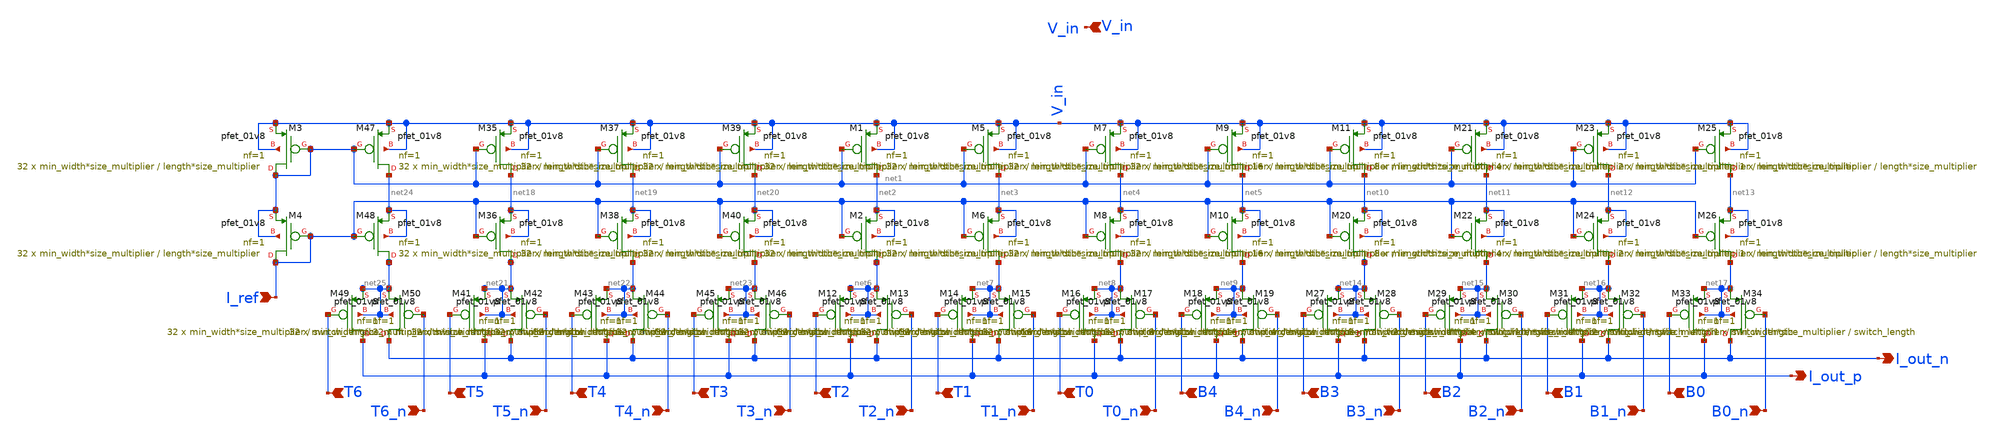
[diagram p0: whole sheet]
** sch_path: analog/schematics/components/DAC/segmented_dac.sch
**.subckt segmented_dac B0 B0_n B1 B2 B3 B1_n B2_n B3_n B4 B4_n T0 T1 T2 T0_n T1_n T2_n I_out_p V_in
*+ I_out_n T3 T4 T5 T3_n T4_n T5_n T6 T6_n I_ref
*.ipin B0
*.ipin B0_n
*.ipin B1
*.ipin B2
*.ipin B3
*.ipin B1_n
*.ipin B2_n
*.ipin B3_n
*.ipin B4
*.ipin B4_n
*.ipin T0
*.ipin T1
*.ipin T2
*.ipin T0_n
*.ipin T1_n
*.ipin T2_n
*.opin I_out_p
*.ipin V_in
*.opin I_out_n
*.ipin T3
*.ipin T4
*.ipin T5
*.ipin T3_n
*.ipin T4_n
*.ipin T5_n
*.ipin T6
*.ipin T6_n
*.ipin I_ref
XM1 net2 net1 V_in V_in sky130_fd_pr__pfet_01v8 L=length*size_multiplier W=min_width*size_multiplier
+ nf=1 ad='int((nf+1)/2) * W/nf * 0.29' as='int((nf+2)/2) * W/nf * 0.29' pd='2*int((nf+1)/2) * (W/nf + 0.29)'
+ ps='2*int((nf+2)/2) * (W/nf + 0.29)' nrd='0.29 / W' nrs='0.29 / W' sa=0 sb=0 sd=0 mult=32 m=32
XM2 net6 I_ref net2 net2 sky130_fd_pr__pfet_01v8 L=length*size_multiplier W=min_width*size_multiplier
+ nf=1 ad='int((nf+1)/2) * W/nf * 0.29' as='int((nf+2)/2) * W/nf * 0.29' pd='2*int((nf+1)/2) * (W/nf + 0.29)'
+ ps='2*int((nf+2)/2) * (W/nf + 0.29)' nrd='0.29 / W' nrs='0.29 / W' sa=0 sb=0 sd=0 mult=32 m=32
XM3 net1 net1 V_in V_in sky130_fd_pr__pfet_01v8 L=length*size_multiplier W=min_width*size_multiplier
+ nf=1 ad='int((nf+1)/2) * W/nf * 0.29' as='int((nf+2)/2) * W/nf * 0.29' pd='2*int((nf+1)/2) * (W/nf + 0.29)'
+ ps='2*int((nf+2)/2) * (W/nf + 0.29)' nrd='0.29 / W' nrs='0.29 / W' sa=0 sb=0 sd=0 mult=32 m=32
XM4 I_ref I_ref net1 net1 sky130_fd_pr__pfet_01v8 L=length*size_multiplier W=min_width*size_multiplier
+ nf=1 ad='int((nf+1)/2) * W/nf * 0.29' as='int((nf+2)/2) * W/nf * 0.29' pd='2*int((nf+1)/2) * (W/nf + 0.29)'
+ ps='2*int((nf+2)/2) * (W/nf + 0.29)' nrd='0.29 / W' nrs='0.29 / W' sa=0 sb=0 sd=0 mult=32 m=32
XM5 net3 net1 V_in V_in sky130_fd_pr__pfet_01v8 L=length*size_multiplier W=min_width*size_multiplier
+ nf=1 ad='int((nf+1)/2) * W/nf * 0.29' as='int((nf+2)/2) * W/nf * 0.29' pd='2*int((nf+1)/2) * (W/nf + 0.29)'
+ ps='2*int((nf+2)/2) * (W/nf + 0.29)' nrd='0.29 / W' nrs='0.29 / W' sa=0 sb=0 sd=0 mult=32 m=32
XM6 net7 I_ref net3 net3 sky130_fd_pr__pfet_01v8 L=length*size_multiplier W=min_width*size_multiplier
+ nf=1 ad='int((nf+1)/2) * W/nf * 0.29' as='int((nf+2)/2) * W/nf * 0.29' pd='2*int((nf+1)/2) * (W/nf + 0.29)'
+ ps='2*int((nf+2)/2) * (W/nf + 0.29)' nrd='0.29 / W' nrs='0.29 / W' sa=0 sb=0 sd=0 mult=32 m=32
XM7 net4 net1 V_in V_in sky130_fd_pr__pfet_01v8 L=length*size_multiplier W=min_width*size_multiplier
+ nf=1 ad='int((nf+1)/2) * W/nf * 0.29' as='int((nf+2)/2) * W/nf * 0.29' pd='2*int((nf+1)/2) * (W/nf + 0.29)'
+ ps='2*int((nf+2)/2) * (W/nf + 0.29)' nrd='0.29 / W' nrs='0.29 / W' sa=0 sb=0 sd=0 mult=32 m=32
XM8 net8 I_ref net4 net4 sky130_fd_pr__pfet_01v8 L=length*size_multiplier W=min_width*size_multiplier
+ nf=1 ad='int((nf+1)/2) * W/nf * 0.29' as='int((nf+2)/2) * W/nf * 0.29' pd='2*int((nf+1)/2) * (W/nf + 0.29)'
+ ps='2*int((nf+2)/2) * (W/nf + 0.29)' nrd='0.29 / W' nrs='0.29 / W' sa=0 sb=0 sd=0 mult=32 m=32
XM9 net5 net1 V_in V_in sky130_fd_pr__pfet_01v8 L=length*size_multiplier W=min_width*size_multiplier
+ nf=1 ad='int((nf+1)/2) * W/nf * 0.29' as='int((nf+2)/2) * W/nf * 0.29' pd='2*int((nf+1)/2) * (W/nf + 0.29)'
+ ps='2*int((nf+2)/2) * (W/nf + 0.29)' nrd='0.29 / W' nrs='0.29 / W' sa=0 sb=0 sd=0 mult=16 m=16
XM10 net9 I_ref net5 net5 sky130_fd_pr__pfet_01v8 L=length*size_multiplier W=min_width*size_multiplier
+ nf=1 ad='int((nf+1)/2) * W/nf * 0.29' as='int((nf+2)/2) * W/nf * 0.29' pd='2*int((nf+1)/2) * (W/nf + 0.29)'
+ ps='2*int((nf+2)/2) * (W/nf + 0.29)' nrd='0.29 / W' nrs='0.29 / W' sa=0 sb=0 sd=0 mult=16 m=16
XM12 I_out_p T2 net6 net6 sky130_fd_pr__pfet_01v8 L=switch_length W=min_width*size_multiplier nf=1 ad='int((nf+1)/2) * W/nf * 0.29'
+ as='int((nf+2)/2) * W/nf * 0.29' pd='2*int((nf+1)/2) * (W/nf + 0.29)' ps='2*int((nf+2)/2) * (W/nf + 0.29)'
+ nrd='0.29 / W' nrs='0.29 / W' sa=0 sb=0 sd=0 mult=32 m=32
XM13 I_out_n T2_n net6 net6 sky130_fd_pr__pfet_01v8 L=switch_length W=min_width*size_multiplier nf=1
+ ad='int((nf+1)/2) * W/nf * 0.29' as='int((nf+2)/2) * W/nf * 0.29' pd='2*int((nf+1)/2) * (W/nf + 0.29)'
+ ps='2*int((nf+2)/2) * (W/nf + 0.29)' nrd='0.29 / W' nrs='0.29 / W' sa=0 sb=0 sd=0 mult=32 m=32
XM14 I_out_p T1 net7 net7 sky130_fd_pr__pfet_01v8 L=switch_length W=min_width*size_multiplier nf=1 ad='int((nf+1)/2) * W/nf * 0.29'
+ as='int((nf+2)/2) * W/nf * 0.29' pd='2*int((nf+1)/2) * (W/nf + 0.29)' ps='2*int((nf+2)/2) * (W/nf + 0.29)'
+ nrd='0.29 / W' nrs='0.29 / W' sa=0 sb=0 sd=0 mult=32 m=32
XM15 I_out_n T1_n net7 net7 sky130_fd_pr__pfet_01v8 L=switch_length W=min_width*size_multiplier nf=1
+ ad='int((nf+1)/2) * W/nf * 0.29' as='int((nf+2)/2) * W/nf * 0.29' pd='2*int((nf+1)/2) * (W/nf + 0.29)'
+ ps='2*int((nf+2)/2) * (W/nf + 0.29)' nrd='0.29 / W' nrs='0.29 / W' sa=0 sb=0 sd=0 mult=32 m=32
XM16 I_out_p T0 net8 net8 sky130_fd_pr__pfet_01v8 L=switch_length W=min_width*size_multiplier nf=1 ad='int((nf+1)/2) * W/nf * 0.29'
+ as='int((nf+2)/2) * W/nf * 0.29' pd='2*int((nf+1)/2) * (W/nf + 0.29)' ps='2*int((nf+2)/2) * (W/nf + 0.29)'
+ nrd='0.29 / W' nrs='0.29 / W' sa=0 sb=0 sd=0 mult=32 m=32
XM17 I_out_n T0_n net8 net8 sky130_fd_pr__pfet_01v8 L=switch_length W=min_width*size_multiplier nf=1
+ ad='int((nf+1)/2) * W/nf * 0.29' as='int((nf+2)/2) * W/nf * 0.29' pd='2*int((nf+1)/2) * (W/nf + 0.29)'
+ ps='2*int((nf+2)/2) * (W/nf + 0.29)' nrd='0.29 / W' nrs='0.29 / W' sa=0 sb=0 sd=0 mult=32 m=32
XM18 I_out_p B4 net9 net9 sky130_fd_pr__pfet_01v8 L=switch_length W=min_width*size_multiplier nf=1 ad='int((nf+1)/2) * W/nf * 0.29'
+ as='int((nf+2)/2) * W/nf * 0.29' pd='2*int((nf+1)/2) * (W/nf + 0.29)' ps='2*int((nf+2)/2) * (W/nf + 0.29)'
+ nrd='0.29 / W' nrs='0.29 / W' sa=0 sb=0 sd=0 mult=16 m=16
XM19 I_out_n B4_n net9 net9 sky130_fd_pr__pfet_01v8 L=switch_length W=min_width*size_multiplier nf=1
+ ad='int((nf+1)/2) * W/nf * 0.29' as='int((nf+2)/2) * W/nf * 0.29' pd='2*int((nf+1)/2) * (W/nf + 0.29)'
+ ps='2*int((nf+2)/2) * (W/nf + 0.29)' nrd='0.29 / W' nrs='0.29 / W' sa=0 sb=0 sd=0 mult=16 m=16
XM11 net10 net1 V_in V_in sky130_fd_pr__pfet_01v8 L=length*size_multiplier W=min_width*size_multiplier
+ nf=1 ad='int((nf+1)/2) * W/nf * 0.29' as='int((nf+2)/2) * W/nf * 0.29' pd='2*int((nf+1)/2) * (W/nf + 0.29)'
+ ps='2*int((nf+2)/2) * (W/nf + 0.29)' nrd='0.29 / W' nrs='0.29 / W' sa=0 sb=0 sd=0 mult=8 m=8
XM20 net14 I_ref net10 net10 sky130_fd_pr__pfet_01v8 L=length*size_multiplier W=min_width*size_multiplier
+ nf=1 ad='int((nf+1)/2) * W/nf * 0.29' as='int((nf+2)/2) * W/nf * 0.29' pd='2*int((nf+1)/2) * (W/nf + 0.29)'
+ ps='2*int((nf+2)/2) * (W/nf + 0.29)' nrd='0.29 / W' nrs='0.29 / W' sa=0 sb=0 sd=0 mult=8 m=8
XM21 net11 net1 V_in V_in sky130_fd_pr__pfet_01v8 L=length*size_multiplier W=min_width*size_multiplier
+ nf=1 ad='int((nf+1)/2) * W/nf * 0.29' as='int((nf+2)/2) * W/nf * 0.29' pd='2*int((nf+1)/2) * (W/nf + 0.29)'
+ ps='2*int((nf+2)/2) * (W/nf + 0.29)' nrd='0.29 / W' nrs='0.29 / W' sa=0 sb=0 sd=0 mult=4 m=4
XM22 net15 I_ref net11 net11 sky130_fd_pr__pfet_01v8 L=length*size_multiplier W=min_width*size_multiplier
+ nf=1 ad='int((nf+1)/2) * W/nf * 0.29' as='int((nf+2)/2) * W/nf * 0.29' pd='2*int((nf+1)/2) * (W/nf + 0.29)'
+ ps='2*int((nf+2)/2) * (W/nf + 0.29)' nrd='0.29 / W' nrs='0.29 / W' sa=0 sb=0 sd=0 mult=4 m=4
XM23 net12 net1 V_in V_in sky130_fd_pr__pfet_01v8 L=length*size_multiplier W=min_width*size_multiplier
+ nf=1 ad='int((nf+1)/2) * W/nf * 0.29' as='int((nf+2)/2) * W/nf * 0.29' pd='2*int((nf+1)/2) * (W/nf + 0.29)'
+ ps='2*int((nf+2)/2) * (W/nf + 0.29)' nrd='0.29 / W' nrs='0.29 / W' sa=0 sb=0 sd=0 mult=2 m=2
XM24 net16 I_ref net12 net12 sky130_fd_pr__pfet_01v8 L=length*size_multiplier W=min_width*size_multiplier
+ nf=1 ad='int((nf+1)/2) * W/nf * 0.29' as='int((nf+2)/2) * W/nf * 0.29' pd='2*int((nf+1)/2) * (W/nf + 0.29)'
+ ps='2*int((nf+2)/2) * (W/nf + 0.29)' nrd='0.29 / W' nrs='0.29 / W' sa=0 sb=0 sd=0 mult=2 m=2
XM25 net13 net1 V_in V_in sky130_fd_pr__pfet_01v8 L=length*size_multiplier W=min_width*size_multiplier
+ nf=1 ad='int((nf+1)/2) * W/nf * 0.29' as='int((nf+2)/2) * W/nf * 0.29' pd='2*int((nf+1)/2) * (W/nf + 0.29)'
+ ps='2*int((nf+2)/2) * (W/nf + 0.29)' nrd='0.29 / W' nrs='0.29 / W' sa=0 sb=0 sd=0 mult=1 m=1
XM26 net17 I_ref net13 net13 sky130_fd_pr__pfet_01v8 L=length*size_multiplier W=min_width*size_multiplier
+ nf=1 ad='int((nf+1)/2) * W/nf * 0.29' as='int((nf+2)/2) * W/nf * 0.29' pd='2*int((nf+1)/2) * (W/nf + 0.29)'
+ ps='2*int((nf+2)/2) * (W/nf + 0.29)' nrd='0.29 / W' nrs='0.29 / W' sa=0 sb=0 sd=0 mult=1 m=1
XM27 I_out_p B3 net14 net14 sky130_fd_pr__pfet_01v8 L=switch_length W=min_width*size_multiplier nf=1
+ ad='int((nf+1)/2) * W/nf * 0.29' as='int((nf+2)/2) * W/nf * 0.29' pd='2*int((nf+1)/2) * (W/nf + 0.29)'
+ ps='2*int((nf+2)/2) * (W/nf + 0.29)' nrd='0.29 / W' nrs='0.29 / W' sa=0 sb=0 sd=0 mult=8 m=8
XM28 I_out_n B3_n net14 net14 sky130_fd_pr__pfet_01v8 L=switch_length W=min_width*size_multiplier nf=1
+ ad='int((nf+1)/2) * W/nf * 0.29' as='int((nf+2)/2) * W/nf * 0.29' pd='2*int((nf+1)/2) * (W/nf + 0.29)'
+ ps='2*int((nf+2)/2) * (W/nf + 0.29)' nrd='0.29 / W' nrs='0.29 / W' sa=0 sb=0 sd=0 mult=8 m=8
XM29 I_out_p B2 net15 net15 sky130_fd_pr__pfet_01v8 L=switch_length W=min_width*size_multiplier nf=1
+ ad='int((nf+1)/2) * W/nf * 0.29' as='int((nf+2)/2) * W/nf * 0.29' pd='2*int((nf+1)/2) * (W/nf + 0.29)'
+ ps='2*int((nf+2)/2) * (W/nf + 0.29)' nrd='0.29 / W' nrs='0.29 / W' sa=0 sb=0 sd=0 mult=4 m=4
XM30 I_out_n B2_n net15 net15 sky130_fd_pr__pfet_01v8 L=switch_length W=min_width*size_multiplier nf=1
+ ad='int((nf+1)/2) * W/nf * 0.29' as='int((nf+2)/2) * W/nf * 0.29' pd='2*int((nf+1)/2) * (W/nf + 0.29)'
+ ps='2*int((nf+2)/2) * (W/nf + 0.29)' nrd='0.29 / W' nrs='0.29 / W' sa=0 sb=0 sd=0 mult=4 m=4
XM31 I_out_p B1 net16 net16 sky130_fd_pr__pfet_01v8 L=switch_length W=min_width*size_multiplier nf=1
+ ad='int((nf+1)/2) * W/nf * 0.29' as='int((nf+2)/2) * W/nf * 0.29' pd='2*int((nf+1)/2) * (W/nf + 0.29)'
+ ps='2*int((nf+2)/2) * (W/nf + 0.29)' nrd='0.29 / W' nrs='0.29 / W' sa=0 sb=0 sd=0 mult=2 m=2
XM32 I_out_n B1_n net16 net16 sky130_fd_pr__pfet_01v8 L=switch_length W=min_width*size_multiplier nf=1
+ ad='int((nf+1)/2) * W/nf * 0.29' as='int((nf+2)/2) * W/nf * 0.29' pd='2*int((nf+1)/2) * (W/nf + 0.29)'
+ ps='2*int((nf+2)/2) * (W/nf + 0.29)' nrd='0.29 / W' nrs='0.29 / W' sa=0 sb=0 sd=0 mult=2 m=2
XM33 I_out_p B0 net17 net17 sky130_fd_pr__pfet_01v8 L=switch_length W=min_width*size_multiplier nf=1
+ ad='int((nf+1)/2) * W/nf * 0.29' as='int((nf+2)/2) * W/nf * 0.29' pd='2*int((nf+1)/2) * (W/nf + 0.29)'
+ ps='2*int((nf+2)/2) * (W/nf + 0.29)' nrd='0.29 / W' nrs='0.29 / W' sa=0 sb=0 sd=0 mult=1 m=1
XM34 I_out_n B0_n net17 net17 sky130_fd_pr__pfet_01v8 L=switch_length W=min_width*size_multiplier nf=1
+ ad='int((nf+1)/2) * W/nf * 0.29' as='int((nf+2)/2) * W/nf * 0.29' pd='2*int((nf+1)/2) * (W/nf + 0.29)'
+ ps='2*int((nf+2)/2) * (W/nf + 0.29)' nrd='0.29 / W' nrs='0.29 / W' sa=0 sb=0 sd=0 mult=1 m=1
XM35 net18 net1 V_in V_in sky130_fd_pr__pfet_01v8 L=length*size_multiplier W=min_width*size_multiplier
+ nf=1 ad='int((nf+1)/2) * W/nf * 0.29' as='int((nf+2)/2) * W/nf * 0.29' pd='2*int((nf+1)/2) * (W/nf + 0.29)'
+ ps='2*int((nf+2)/2) * (W/nf + 0.29)' nrd='0.29 / W' nrs='0.29 / W' sa=0 sb=0 sd=0 mult=32 m=32
XM36 net21 I_ref net18 net18 sky130_fd_pr__pfet_01v8 L=length*size_multiplier W=min_width*size_multiplier
+ nf=1 ad='int((nf+1)/2) * W/nf * 0.29' as='int((nf+2)/2) * W/nf * 0.29' pd='2*int((nf+1)/2) * (W/nf + 0.29)'
+ ps='2*int((nf+2)/2) * (W/nf + 0.29)' nrd='0.29 / W' nrs='0.29 / W' sa=0 sb=0 sd=0 mult=32 m=32
XM37 net19 net1 V_in V_in sky130_fd_pr__pfet_01v8 L=length*size_multiplier W=min_width*size_multiplier
+ nf=1 ad='int((nf+1)/2) * W/nf * 0.29' as='int((nf+2)/2) * W/nf * 0.29' pd='2*int((nf+1)/2) * (W/nf + 0.29)'
+ ps='2*int((nf+2)/2) * (W/nf + 0.29)' nrd='0.29 / W' nrs='0.29 / W' sa=0 sb=0 sd=0 mult=32 m=32
XM38 net22 I_ref net19 net19 sky130_fd_pr__pfet_01v8 L=length*size_multiplier W=min_width*size_multiplier
+ nf=1 ad='int((nf+1)/2) * W/nf * 0.29' as='int((nf+2)/2) * W/nf * 0.29' pd='2*int((nf+1)/2) * (W/nf + 0.29)'
+ ps='2*int((nf+2)/2) * (W/nf + 0.29)' nrd='0.29 / W' nrs='0.29 / W' sa=0 sb=0 sd=0 mult=32 m=32
XM39 net20 net1 V_in V_in sky130_fd_pr__pfet_01v8 L=length*size_multiplier W=min_width*size_multiplier
+ nf=1 ad='int((nf+1)/2) * W/nf * 0.29' as='int((nf+2)/2) * W/nf * 0.29' pd='2*int((nf+1)/2) * (W/nf + 0.29)'
+ ps='2*int((nf+2)/2) * (W/nf + 0.29)' nrd='0.29 / W' nrs='0.29 / W' sa=0 sb=0 sd=0 mult=32 m=32
XM40 net23 I_ref net20 net20 sky130_fd_pr__pfet_01v8 L=length*size_multiplier W=min_width*size_multiplier
+ nf=1 ad='int((nf+1)/2) * W/nf * 0.29' as='int((nf+2)/2) * W/nf * 0.29' pd='2*int((nf+1)/2) * (W/nf + 0.29)'
+ ps='2*int((nf+2)/2) * (W/nf + 0.29)' nrd='0.29 / W' nrs='0.29 / W' sa=0 sb=0 sd=0 mult=32 m=32
XM41 I_out_p T5 net21 net21 sky130_fd_pr__pfet_01v8 L=switch_length W=min_width*size_multiplier nf=1
+ ad='int((nf+1)/2) * W/nf * 0.29' as='int((nf+2)/2) * W/nf * 0.29' pd='2*int((nf+1)/2) * (W/nf + 0.29)'
+ ps='2*int((nf+2)/2) * (W/nf + 0.29)' nrd='0.29 / W' nrs='0.29 / W' sa=0 sb=0 sd=0 mult=32 m=32
XM42 I_out_n T5_n net21 net21 sky130_fd_pr__pfet_01v8 L=switch_length W=min_width*size_multiplier nf=1
+ ad='int((nf+1)/2) * W/nf * 0.29' as='int((nf+2)/2) * W/nf * 0.29' pd='2*int((nf+1)/2) * (W/nf + 0.29)'
+ ps='2*int((nf+2)/2) * (W/nf + 0.29)' nrd='0.29 / W' nrs='0.29 / W' sa=0 sb=0 sd=0 mult=32 m=32
XM43 I_out_p T4 net22 net22 sky130_fd_pr__pfet_01v8 L=switch_length W=min_width*size_multiplier nf=1
+ ad='int((nf+1)/2) * W/nf * 0.29' as='int((nf+2)/2) * W/nf * 0.29' pd='2*int((nf+1)/2) * (W/nf + 0.29)'
+ ps='2*int((nf+2)/2) * (W/nf + 0.29)' nrd='0.29 / W' nrs='0.29 / W' sa=0 sb=0 sd=0 mult=32 m=32
XM44 I_out_n T4_n net22 net22 sky130_fd_pr__pfet_01v8 L=switch_length W=min_width*size_multiplier nf=1
+ ad='int((nf+1)/2) * W/nf * 0.29' as='int((nf+2)/2) * W/nf * 0.29' pd='2*int((nf+1)/2) * (W/nf + 0.29)'
+ ps='2*int((nf+2)/2) * (W/nf + 0.29)' nrd='0.29 / W' nrs='0.29 / W' sa=0 sb=0 sd=0 mult=32 m=32
XM45 I_out_p T3 net23 net23 sky130_fd_pr__pfet_01v8 L=switch_length W=min_width*size_multiplier nf=1
+ ad='int((nf+1)/2) * W/nf * 0.29' as='int((nf+2)/2) * W/nf * 0.29' pd='2*int((nf+1)/2) * (W/nf + 0.29)'
+ ps='2*int((nf+2)/2) * (W/nf + 0.29)' nrd='0.29 / W' nrs='0.29 / W' sa=0 sb=0 sd=0 mult=32 m=32
XM46 I_out_n T3_n net23 net23 sky130_fd_pr__pfet_01v8 L=switch_length W=min_width*size_multiplier nf=1
+ ad='int((nf+1)/2) * W/nf * 0.29' as='int((nf+2)/2) * W/nf * 0.29' pd='2*int((nf+1)/2) * (W/nf + 0.29)'
+ ps='2*int((nf+2)/2) * (W/nf + 0.29)' nrd='0.29 / W' nrs='0.29 / W' sa=0 sb=0 sd=0 mult=32 m=32
XM47 net24 net1 V_in V_in sky130_fd_pr__pfet_01v8 L=length*size_multiplier W=min_width*size_multiplier
+ nf=1 ad='int((nf+1)/2) * W/nf * 0.29' as='int((nf+2)/2) * W/nf * 0.29' pd='2*int((nf+1)/2) * (W/nf + 0.29)'
+ ps='2*int((nf+2)/2) * (W/nf + 0.29)' nrd='0.29 / W' nrs='0.29 / W' sa=0 sb=0 sd=0 mult=32 m=32
XM48 net25 I_ref net24 net24 sky130_fd_pr__pfet_01v8 L=length*size_multiplier W=min_width*size_multiplier
+ nf=1 ad='int((nf+1)/2) * W/nf * 0.29' as='int((nf+2)/2) * W/nf * 0.29' pd='2*int((nf+1)/2) * (W/nf + 0.29)'
+ ps='2*int((nf+2)/2) * (W/nf + 0.29)' nrd='0.29 / W' nrs='0.29 / W' sa=0 sb=0 sd=0 mult=32 m=32
XM49 I_out_p T6 net25 net25 sky130_fd_pr__pfet_01v8 L=switch_length W=min_width*size_multiplier nf=1
+ ad='int((nf+1)/2) * W/nf * 0.29' as='int((nf+2)/2) * W/nf * 0.29' pd='2*int((nf+1)/2) * (W/nf + 0.29)'
+ ps='2*int((nf+2)/2) * (W/nf + 0.29)' nrd='0.29 / W' nrs='0.29 / W' sa=0 sb=0 sd=0 mult=32 m=32
XM50 I_out_n T6_n net25 net25 sky130_fd_pr__pfet_01v8 L=switch_length W=min_width*size_multiplier nf=1
+ ad='int((nf+1)/2) * W/nf * 0.29' as='int((nf+2)/2) * W/nf * 0.29' pd='2*int((nf+1)/2) * (W/nf + 0.29)'
+ ps='2*int((nf+2)/2) * (W/nf + 0.29)' nrd='0.29 / W' nrs='0.29 / W' sa=0 sb=0 sd=0 mult=32 m=32
**** begin user architecture code

.param min_width=0.42
.param switch_multiplier=1
.param length=0.425
.param switch_length=0.15
.param size_multiplier=10

**** end user architecture code
**.ends
.end
